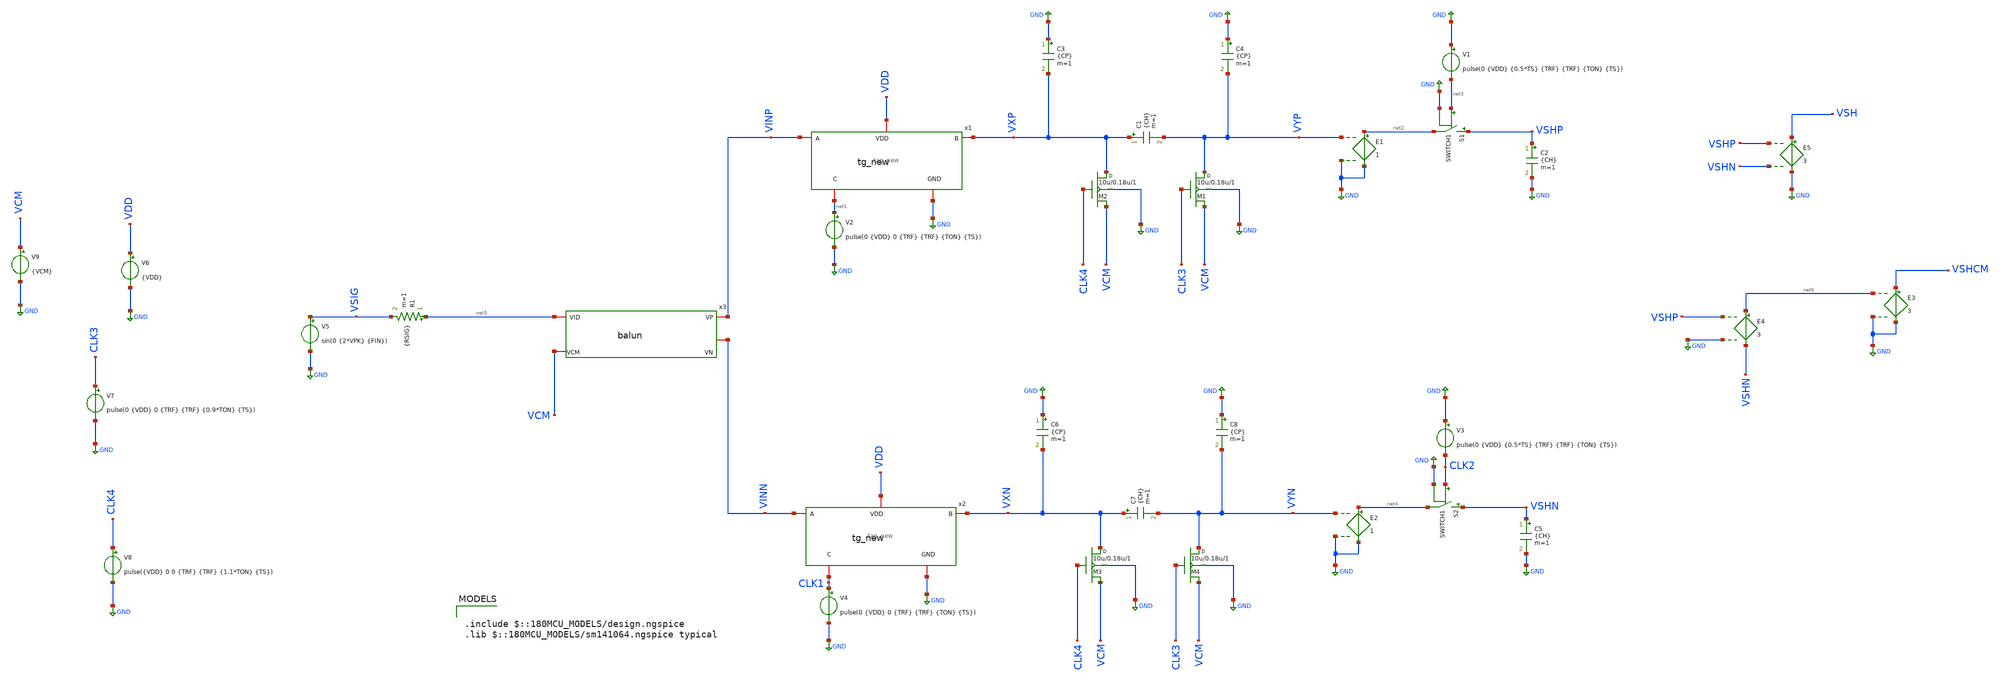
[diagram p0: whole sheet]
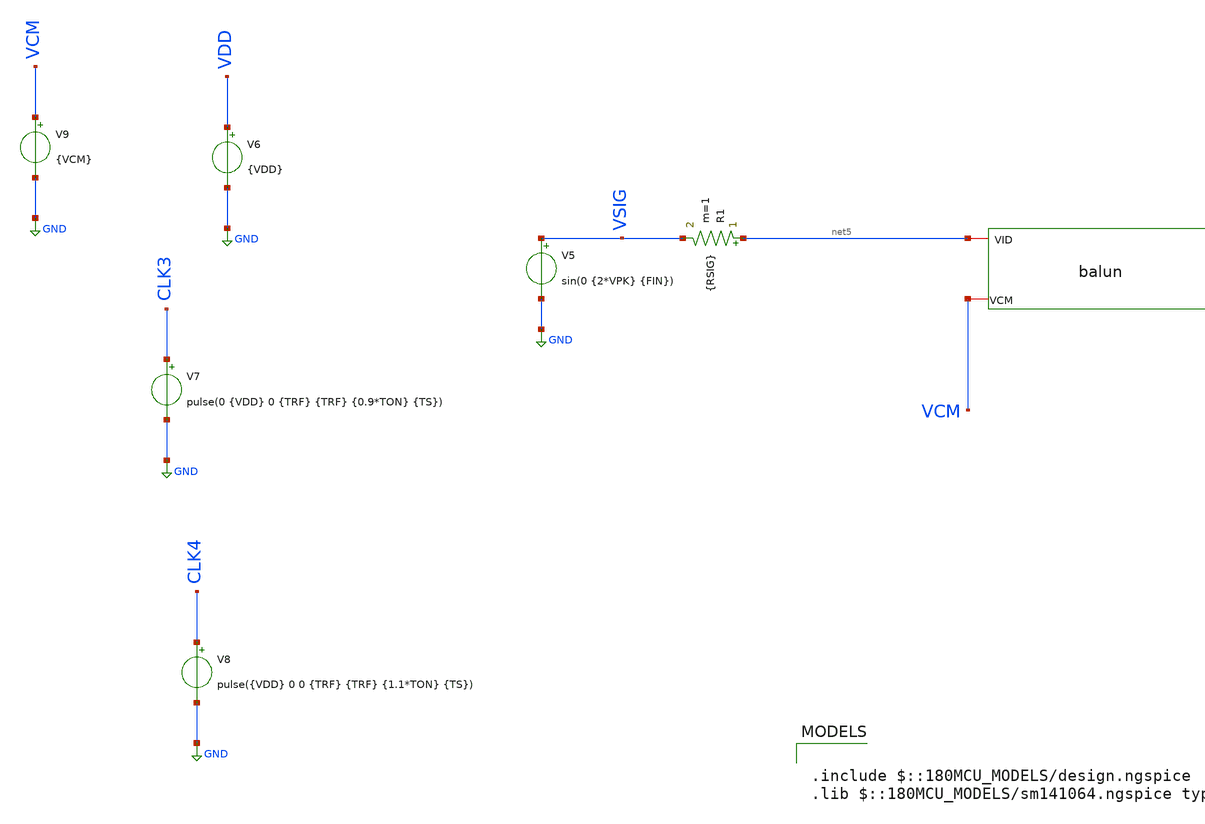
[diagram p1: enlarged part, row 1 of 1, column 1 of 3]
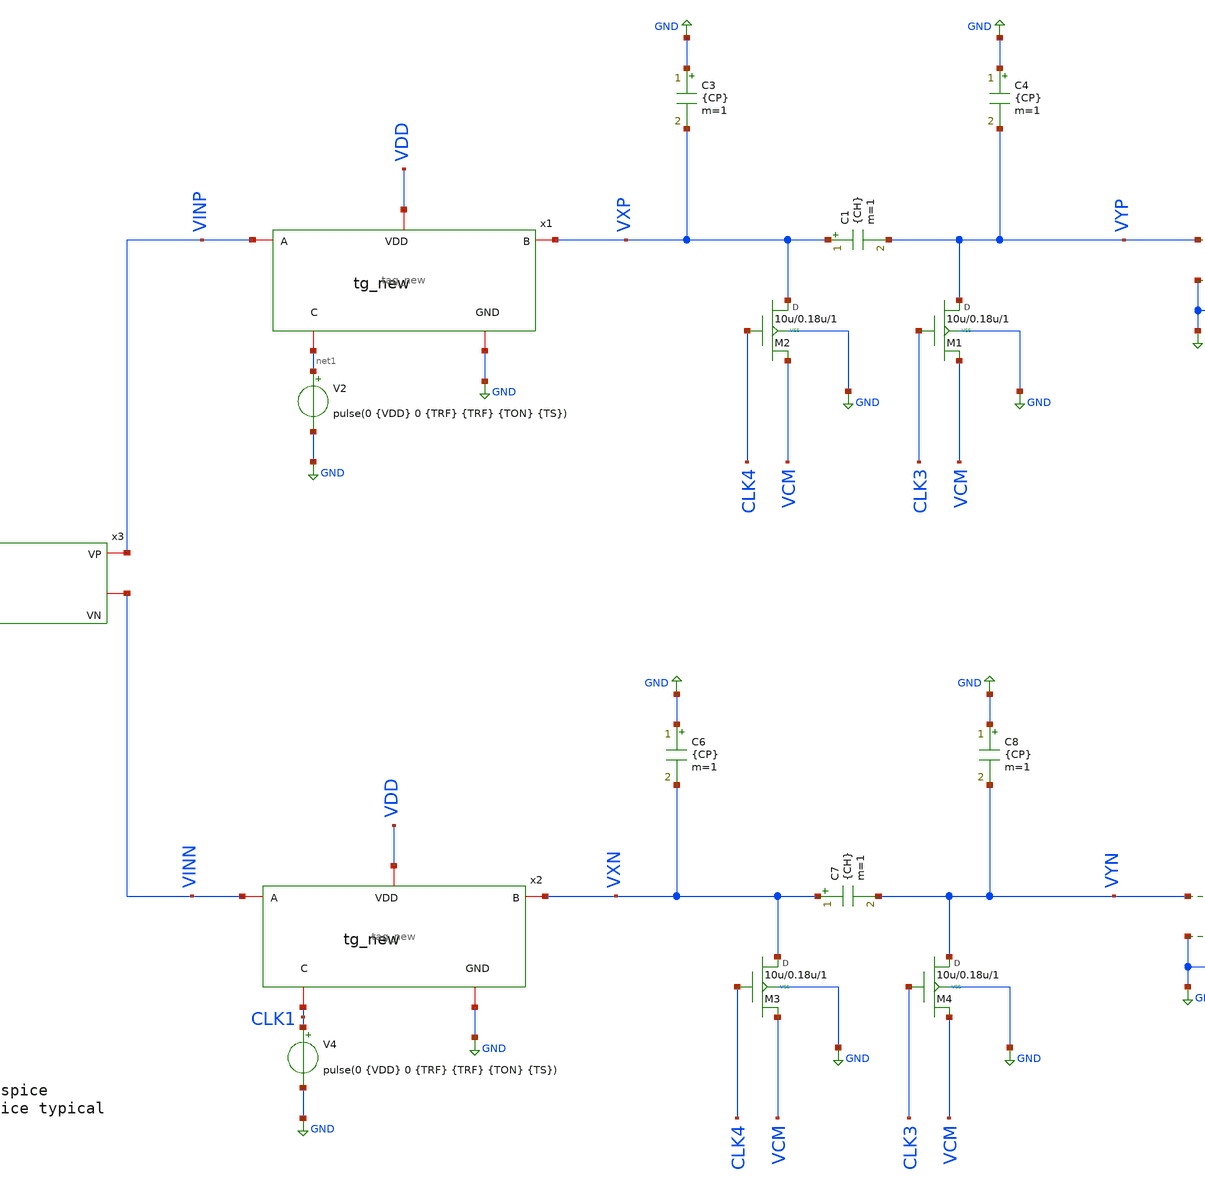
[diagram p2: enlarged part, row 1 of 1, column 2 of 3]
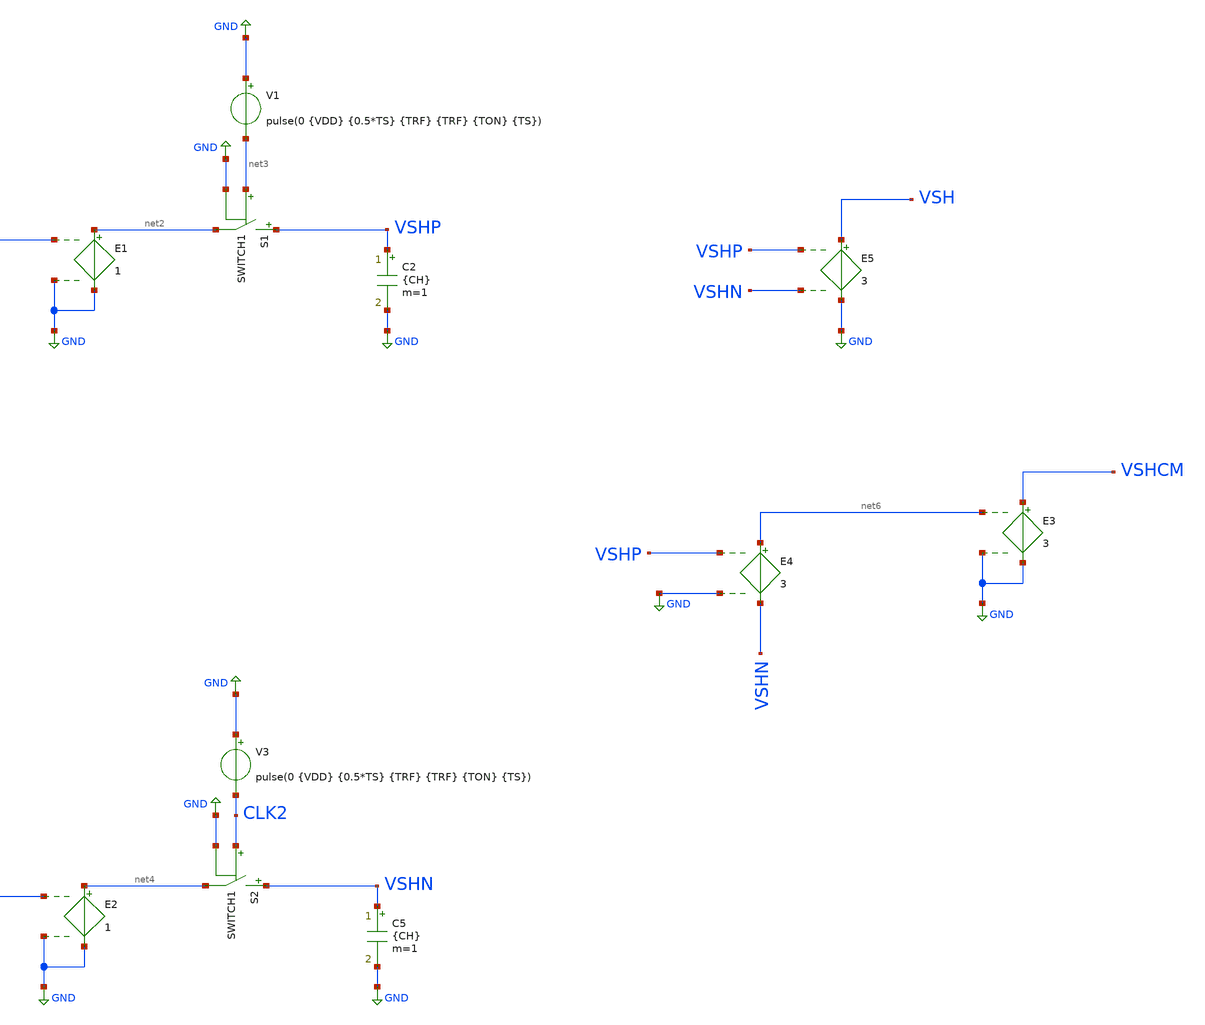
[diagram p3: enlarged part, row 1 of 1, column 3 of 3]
** sch_path: Designs/lab3_part3.sch
**.subckt lab3_part3
E1 net2 GND VYP GND 1
S1 VSHP net2 net3 GND SWITCH1
C2 VSHP GND {CH} m=1
V1 GND net3 pulse(0 {VDD} {0.5*TS} {TRF} {TRF} {TON} {TS})
V2 net1 GND pulse(0 {VDD} 0 {TRF} {TRF} {TON} {TS})
x1 net1 GND VINP VXP VDD tag_new W_N=10u L_N=0.18u W_P=10u L_P=0.18u
C3 GND VXP {CP} m=1
M2 VXP CLK4 VCM VSS nmos w=10u l=0.18u m=1
C1 VXP VYP {CH} m=1
C4 GND VYP {CP} m=1
M1 VYP CLK3 VCM VSS nmos w=10u l=0.18u m=1
E2 net4 GND VYN GND 1
S2 VSHN net4 CLK2 GND SWITCH1
C5 VSHN GND {CH} m=1
V3 GND CLK2 pulse(0 {VDD} {0.5*TS} {TRF} {TRF} {TON} {TS})
V4 CLK1 GND pulse(0 {VDD} 0 {TRF} {TRF} {TON} {TS})
x2 CLK1 GND VINN VXN VDD tag_new W_N=10u L_N=0.18u W_P=10u L_P=0.18u
C6 GND VXN {CP} m=1
M3 VXN CLK4 VCM VSS nmos w=10u l=0.18u m=1
C7 VXN VYN {CH} m=1
C8 GND VYN {CP} m=1
M4 VYN CLK3 VCM VSS nmos w=10u l=0.18u m=1
x3 VINP VCM VINN net5 balun
R1 net5 VSIG {RSIG} m=1
V5 VSIG GND sin(0 {2*VPK} {FIN})
V6 VDD GND {VDD}
V7 CLK3 GND pulse(0 {VDD} 0 {TRF} {TRF} {0.9*TON} {TS})
V8 CLK4 GND pulse({VDD} 0 0 {TRF} {TRF} {1.1*TON} {TS})
V9 VCM GND {VCM}
E3 VSHCM GND net6 GND 3
E4 net6 VSHN VSHP GND 3
E5 VSH GND VSHP VSHN 3
**** begin user architecture code

.include $::180MCU_MODELS/design.ngspice
.lib $::180MCU_MODELS/sm141064.ngspice typical





*These are the values of the parameters to be used
.param TS=1u
.param CH=1p CP={0.1*CH} RSIG=1k TON={0.4*TS} TRF=1n NCYC=5 NFFT=256 FIN={(NCYC/NFFT)/TS}
.param VDD=2 VDC={VDD/2} VCM={VDD/2} VPK={VDD/4} TDROP={0.5/FIN} TSTOP={(NCYC/FIN)+TDROP}
.param W_N=10u L_N=0.28u W_P=10u L_P=0.28u

*Analysis setup and control statements
.tran 25n {TSTOP} {TDROP}
.options filetype=ascii
*.options reltol=0.1u vntol=0.11u abstol=1p

*Required model for the switch
.model SWITCH1 sw vt={VDD/2}

.model nmos nmos

*save all voltages and currents
.save all



**** end user architecture code
**.ends

* expanding   symbol:  /home/tare/Desktop/Analog design/tag_new.sym # of pins=5
** sym_path: Designs/tag_new.sym
** sch_path: Designs/tag_new.sch
.subckt tag_new C GND A B VDD  W_N=10u L_N=0.18u W_P=10u L_P=0.18u
*.iopin B
*.iopin GND
*.iopin A
*.iopin VDD
*.iopin C
E1 net1 VDD C GND -1
XM3 B C A GND nmos_3p3_sab L=0.28u W=10u nf=1 ad='int((nf+1)/2) * W/nf * 0.18u' as='int((nf+2)/2) * W/nf * 0.18u'
+ pd='2*int((nf+1)/2) * (W/nf + 0.18u)' ps='2*int((nf+2)/2) * (W/nf + 0.18u)' nrd='0.18u / W' nrs='0.18u / W'
+ sa=0 sb=0 sd=0 m=1
XM1 B net1 A VDD pmos_3p3_sab L=0.28u W=10u nf=1 ad='int((nf+1)/2) * W/nf * 0.18u' as='int((nf+2)/2) * W/nf * 0.18u'
+ pd='2*int((nf+1)/2) * (W/nf + 0.18u)' ps='2*int((nf+2)/2) * (W/nf + 0.18u)' nrd='0.18u / W' nrs='0.18u / W'
+ sa=0 sb=0 sd=0 m=1
.ends


* expanding   symbol:  /home/tare/Desktop/Analog design/balun.sym # of pins=4
** sym_path: Designs/balun.sym
** sch_path: Designs/balun.sch
.subckt balun VP VCM VID VN
*.iopin VP
*.iopin VCM
*.iopin VN
*.iopin VID
E2 VP VCM net1 GND 0.5
E3 VN VCM net1 GND -0.5
E1 net1 GND VID GND 1
.ends

.GLOBAL GND
.end
